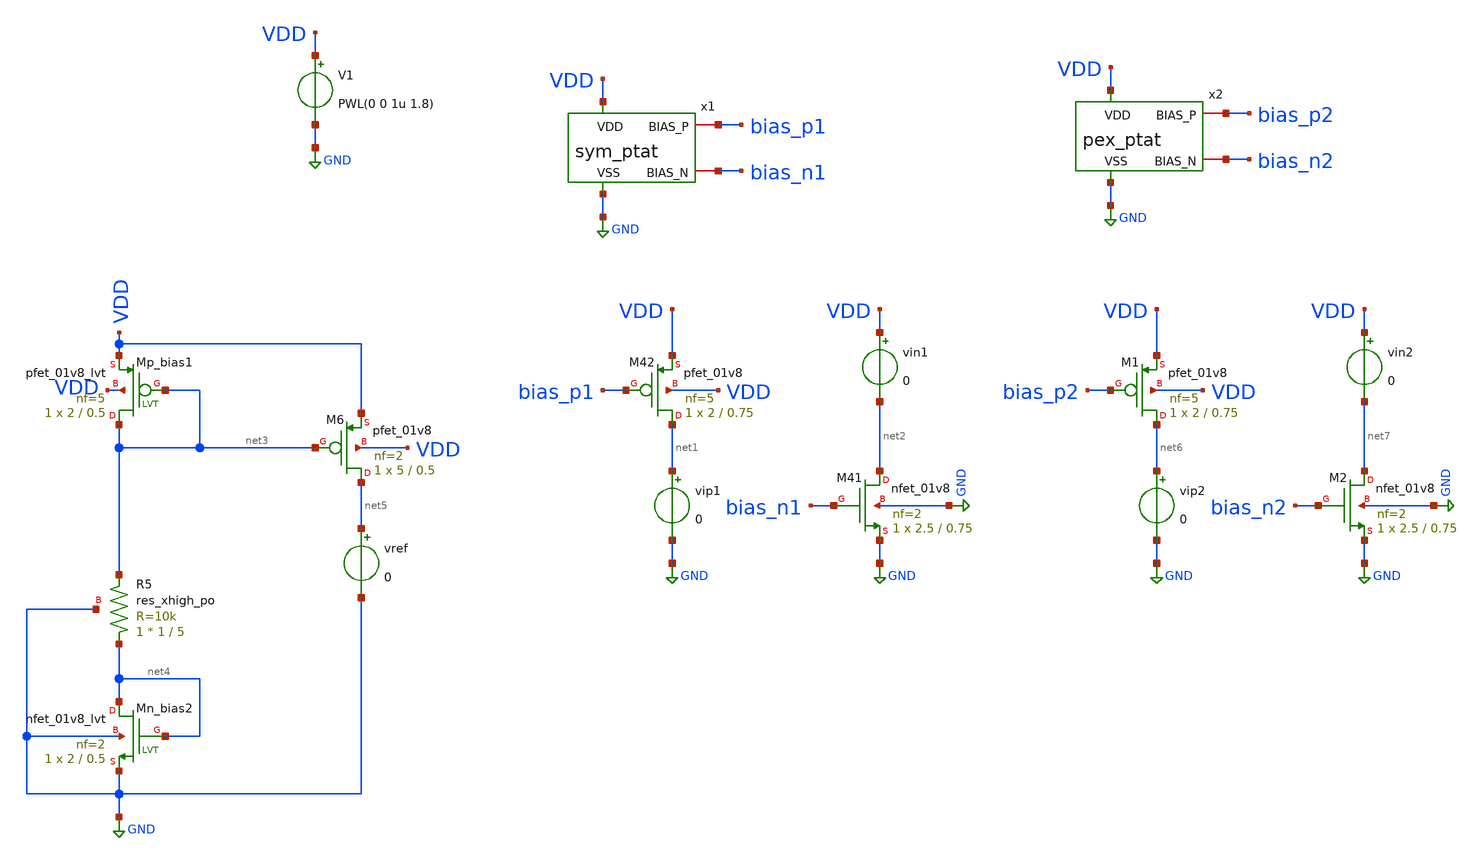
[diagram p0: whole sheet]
** sch_path: schem/tb/tb_ptat.sch
**.subckt tb_ptat
V1 VDD GND PWL(0 0 1u 1.8)
XM42 net1 bias_p1 VDD VDD sky130_fd_pr__pfet_01v8 L=0.75 W=2 nf=5 ad='int((5 + 1)/2) * 2 / 5 * 0.29'
+ as='int((5 + 2)/2) * 2 / 5 * 0.29' pd='2*int((5 + 1)/2) * (2 / 5 + 0.29)' ps='2*int((5 + 2)/2) * (2 / 5 + 0.29)'
+ nrd='0.29 / 2 ' nrs='0.29 / 2 ' sa=0 sb=0 sd=0 mult=1 m=1
vip1 net1 GND 0
XM41 net2 bias_n1 GND GND sky130_fd_pr__nfet_01v8 L=0.75 W=2.5 nf=2 ad='int((2 + 1)/2) * 2.5 / 2 * 0.29'
+ as='int((2 + 2)/2) * 2.5 / 2 * 0.29' pd='2*int((2 + 1)/2) * (2.5 / 2 + 0.29)' ps='2*int((2 + 2)/2) * (2.5 / 2 + 0.29)'
+ nrd='0.29 / 2.5 ' nrs='0.29 / 2.5 ' sa=0 sb=0 sd=0 mult=1 m=1
vin1 VDD net2 0
XM6 net5 net3 VDD VDD sky130_fd_pr__pfet_01v8 L=0.5 W=5 nf=2 ad='int((2 + 1)/2) * 5 / 2 * 0.29' as='int((2 + 2)/2) * 5 / 2 * 0.29'
+ pd='2*int((2 + 1)/2) * (5 / 2 + 0.29)' ps='2*int((2 + 2)/2) * (5 / 2 + 0.29)' nrd='0.29 / 5 ' nrs='0.29 / 5 '
+ sa=0 sb=0 sd=0 mult=1 m=1
vref net5 GND 0
XMn_bias2 net4 net4 GND GND sky130_fd_pr__nfet_01v8_lvt L=0.5 W=2 nf=2 ad='int((nf+1)/2) * W/nf * 0.29'
+ as='int((nf+2)/2) * W/nf * 0.29' pd='2*int((nf+1)/2) * (W/nf + 0.29)' ps='2*int((nf+2)/2) * (W/nf + 0.29)'
+ nrd='0.29 / W' nrs='0.29 / W' sa=0 sb=0 sd=0 mult=1 m=1
XMp_bias1 net3 net3 VDD VDD sky130_fd_pr__pfet_01v8_lvt L=0.5 W=2 nf=5 ad='int((nf+1)/2) * W/nf * 0.29'
+ as='int((nf+2)/2) * W/nf * 0.29' pd='2*int((nf+1)/2) * (W/nf + 0.29)' ps='2*int((nf+2)/2) * (W/nf + 0.29)'
+ nrd='0.29 / W' nrs='0.29 / W' sa=0 sb=0 sd=0 mult=1 m=1
XR5 net4 net3 GND sky130_fd_pr__res_xhigh_po W=1 L=5 mult=1 m=1
XM1 net6 bias_p2 VDD VDD sky130_fd_pr__pfet_01v8 L=0.75 W=2 nf=5 ad='int((5 + 1)/2) * 2 / 5 * 0.29' as='int((5 + 2)/2) * 2 / 5 * 0.29'
+ pd='2*int((5 + 1)/2) * (2 / 5 + 0.29)' ps='2*int((5 + 2)/2) * (2 / 5 + 0.29)' nrd='0.29 / 2 ' nrs='0.29 / 2 '
+ sa=0 sb=0 sd=0 mult=1 m=1
vip2 net6 GND 0
XM2 net7 bias_n2 GND GND sky130_fd_pr__nfet_01v8 L=0.75 W=2.5 nf=2 ad='int((2 + 1)/2) * 2.5 / 2 * 0.29'
+ as='int((2 + 2)/2) * 2.5 / 2 * 0.29' pd='2*int((2 + 1)/2) * (2.5 / 2 + 0.29)' ps='2*int((2 + 2)/2) * (2.5 / 2 + 0.29)'
+ nrd='0.29 / 2.5 ' nrs='0.29 / 2.5 ' sa=0 sb=0 sd=0 mult=1 m=1
vin2 VDD net7 0
x1 VDD GND bias_p1 bias_n1 sym_ptat
x2 VDD GND bias_p2 bias_n2 ptat
**** begin user architecture code


.include /home/zhixuan/projects/fyp_vco/magic/ip/ptat/ptat.spice
.lib /usr/local/share/pdk/sky130A/libs.tech/ngspice/sky130.lib.spice tt
.save all
.control
  set noaskquit
  let n = 34
  let tvec = vector(n)
  let ivec1p = vector(n)
  let ivec1n = vector(n)
  let ivec2p = vector(n)
  let ivec2n = vector(n)
  let refvec = vector(n)
  let idx = 0
  foreach t -40 -35 -30 -25 -20 -15 -10 -5 0 5 10 15 20 25 30 35 40 45 50 55 60 65 70 75 80 85 90 95
+ 100 105 110 115 120 125
    set temp = $t
    tran 10n 10u
    let tvec[idx] = $t
    let ivec1p[idx] = i(vip1)[length(i(vip1))-1]
    let ivec1n[idx] = i(vin1)[length(i(vin1))-1]
    let ivec2p[idx] = i(vip2)[length(i(vip2))-1]
    let ivec2n[idx] = i(vin2)[length(i(vin2))-1]
    let refvec[idx] = i(vref)[length(i(vref))-1]
    let idx = idx + 1
  end
  plot ivec1p ivec1n refvec ivec2p ivec2n vs tvec

  echo "temp ivec1p ivec1n refvec" > /home/zhixuan/projects/fyp_vco/schem/tb/ptat_tb_out1.txt
  print col tvec ivec1p ivec1n refvec >> /home/zhixuan/projects/fyp_vco/schem/tb/ptat_tb_out1.txt
  echo "temp ivec2p ivec2n refvec" > /home/zhixuan/projects/fyp_vco/schem/tb/ptat_tb_out2.txt
  print col tvec ivec2p ivec2n refvec >> /home/zhixuan/projects/fyp_vco/schem/tb/ptat_tb_out2.txt
.endc
.end


**** end user architecture code
**.ends

* expanding   symbol:  /home/zhixuan/projects/fyp_vco/schem/symbol_repo/sym_ptat.sym # of pins=4
** sym_path: schem/symbol_repo/sym_ptat.sym
** sch_path: schem/symbol_repo/sym_ptat.sch
.subckt sym_ptat VDD VSS BIAS_P BIAS_N
*.ipin VDD
*.ipin VSS
*.iopin BIAS_P
*.iopin BIAS_N
XMN_ptat2 net6 net1 net2 VSS sky130_fd_pr__nfet_01v8 L=0.5 W=2 nf=2 ad='int((2 + 1)/2) * 2 / 2 * 0.29'
+ as='int((2 + 2)/2) * 2 / 2 * 0.29' pd='2*int((2 + 1)/2) * (2 / 2 + 0.29)' ps='2*int((2 + 2)/2) * (2 / 2 + 0.29)'
+ nrd='0.29 / 2 ' nrs='0.29 / 2 ' sa=0 sb=0 sd=0 mult=1 m=1
XMP_diode1 net3 BIAS_P VDD VDD sky130_fd_pr__pfet_01v8 L=0.5 W=2 nf=2 ad='int((2 + 1)/2) * 2 / 2 * 0.29'
+ as='int((2 + 2)/2) * 2 / 2 * 0.29' pd='2*int((2 + 1)/2) * (2 / 2 + 0.29)' ps='2*int((2 + 2)/2) * (2 / 2 + 0.29)'
+ nrd='0.29 / 2 ' nrs='0.29 / 2 ' sa=0 sb=0 sd=0 mult=1 m=1
XMP_mir1_l net4 BIAS_P VDD VDD sky130_fd_pr__pfet_01v8 L=0.5 W=2 nf=2 ad='int((2 + 1)/2) * 2 / 2 * 0.29'
+ as='int((2 + 2)/2) * 2 / 2 * 0.29' pd='2*int((2 + 1)/2) * (2 / 2 + 0.29)' ps='2*int((2 + 2)/2) * (2 / 2 + 0.29)'
+ nrd='0.29 / 2 ' nrs='0.29 / 2 ' sa=0 sb=0 sd=0 mult=1 m=1
XMN_diode2 net5 net1 VSS VSS sky130_fd_pr__nfet_01v8 L=0.5 W=2 nf=4 ad='int((4 + 1)/2) * 2 / 4 * 0.29'
+ as='int((4 + 2)/2) * 2 / 4 * 0.29' pd='2*int((4 + 1)/2) * (2 / 4 + 0.29)' ps='2*int((4 + 2)/2) * (2 / 4 + 0.29)'
+ nrd='0.29 / 2 ' nrs='0.29 / 2 ' sa=0 sb=0 sd=0 mult=1 m=1
XMP_inv BIAS_N BIAS_P VDD VDD sky130_fd_pr__pfet_01v8 L=0.75 W=2 nf=5 ad='int((5 + 1)/2) * 2 / 5 * 0.29'
+ as='int((5 + 2)/2) * 2 / 5 * 0.29' pd='2*int((5 + 1)/2) * (2 / 5 + 0.29)' ps='2*int((5 + 2)/2) * (2 / 5 + 0.29)'
+ nrd='0.29 / 2 ' nrs='0.29 / 2 ' sa=0 sb=0 sd=0 mult=1 m=1
XMP_diode2 BIAS_P BIAS_P net3 VDD sky130_fd_pr__pfet_01v8 L=0.5 W=2 nf=2 ad='int((2 + 1)/2) * 2 / 2 * 0.29'
+ as='int((2 + 2)/2) * 2 / 2 * 0.29' pd='2*int((2 + 1)/2) * (2 / 2 + 0.29)' ps='2*int((2 + 2)/2) * (2 / 2 + 0.29)'
+ nrd='0.29 / 2 ' nrs='0.29 / 2 ' sa=0 sb=0 sd=0 mult=1 m=1
XMP_mir2_l net1 BIAS_P net4 VDD sky130_fd_pr__pfet_01v8 L=0.5 W=2 nf=2 ad='int((2 + 1)/2) * 2 / 2 * 0.29'
+ as='int((2 + 2)/2) * 2 / 2 * 0.29' pd='2*int((2 + 1)/2) * (2 / 2 + 0.29)' ps='2*int((2 + 2)/2) * (2 / 2 + 0.29)'
+ nrd='0.29 / 2 ' nrs='0.29 / 2 ' sa=0 sb=0 sd=0 mult=1 m=1
XMN_ptat1 BIAS_P net1 net6 VSS sky130_fd_pr__nfet_01v8 L=0.5 W=2 nf=2 ad='int((2 + 1)/2) * 2 / 2 * 0.29'
+ as='int((2 + 2)/2) * 2 / 2 * 0.29' pd='2*int((2 + 1)/2) * (2 / 2 + 0.29)' ps='2*int((2 + 2)/2) * (2 / 2 + 0.29)'
+ nrd='0.29 / 2 ' nrs='0.29 / 2 ' sa=0 sb=0 sd=0 mult=1 m=1
XMN_diode1 net1 net1 net5 VSS sky130_fd_pr__nfet_01v8 L=0.5 W=2 nf=4 ad='int((4 + 1)/2) * 2 / 4 * 0.29'
+ as='int((4 + 2)/2) * 2 / 4 * 0.29' pd='2*int((4 + 1)/2) * (2 / 4 + 0.29)' ps='2*int((4 + 2)/2) * (2 / 4 + 0.29)'
+ nrd='0.29 / 2 ' nrs='0.29 / 2 ' sa=0 sb=0 sd=0 mult=1 m=1
XMN_inv BIAS_N BIAS_N VSS VSS sky130_fd_pr__nfet_01v8 L=0.75 W=2.5 nf=2 ad='int((2 + 1)/2) * 2.5 / 2 * 0.29'
+ as='int((2 + 2)/2) * 2.5 / 2 * 0.29' pd='2*int((2 + 1)/2) * (2.5 / 2 + 0.29)' ps='2*int((2 + 2)/2) * (2.5 / 2 + 0.29)'
+ nrd='0.29 / 2.5 ' nrs='0.29 / 2.5 ' sa=0 sb=0 sd=0 mult=1 m=1
XR1 VSS net2 VSS sky130_fd_pr__res_xhigh_po_0p35 L=2.8 mult=1 m=1
XMP_startup net1 VSS VDD VDD sky130_fd_pr__pfet_01v8 L=13 W=1 nf=1 ad='int((1 + 1)/2) * 1 / 1 * 0.29'
+ as='int((1 + 2)/2) * 1 / 1 * 0.29' pd='2*int((1 + 1)/2) * (1 / 1 + 0.29)' ps='2*int((1 + 2)/2) * (1 / 1 + 0.29)'
+ nrd='0.29 / 1 ' nrs='0.29 / 1 ' sa=0 sb=0 sd=0 mult=1 m=1
XMN_diode3 net7 net1 VSS VSS sky130_fd_pr__nfet_01v8 L=0.5 W=2 nf=4 ad='int((4 + 1)/2) * 2 / 4 * 0.29'
+ as='int((4 + 2)/2) * 2 / 4 * 0.29' pd='2*int((4 + 1)/2) * (2 / 4 + 0.29)' ps='2*int((4 + 2)/2) * (2 / 4 + 0.29)'
+ nrd='0.29 / 2 ' nrs='0.29 / 2 ' sa=0 sb=0 sd=0 mult=1 m=1
XMN_diode4 net1 net1 net7 VSS sky130_fd_pr__nfet_01v8 L=0.5 W=2 nf=4 ad='int((4 + 1)/2) * 2 / 4 * 0.29'
+ as='int((4 + 2)/2) * 2 / 4 * 0.29' pd='2*int((4 + 1)/2) * (2 / 4 + 0.29)' ps='2*int((4 + 2)/2) * (2 / 4 + 0.29)'
+ nrd='0.29 / 2 ' nrs='0.29 / 2 ' sa=0 sb=0 sd=0 mult=1 m=1
.ends

.GLOBAL GND
.end
